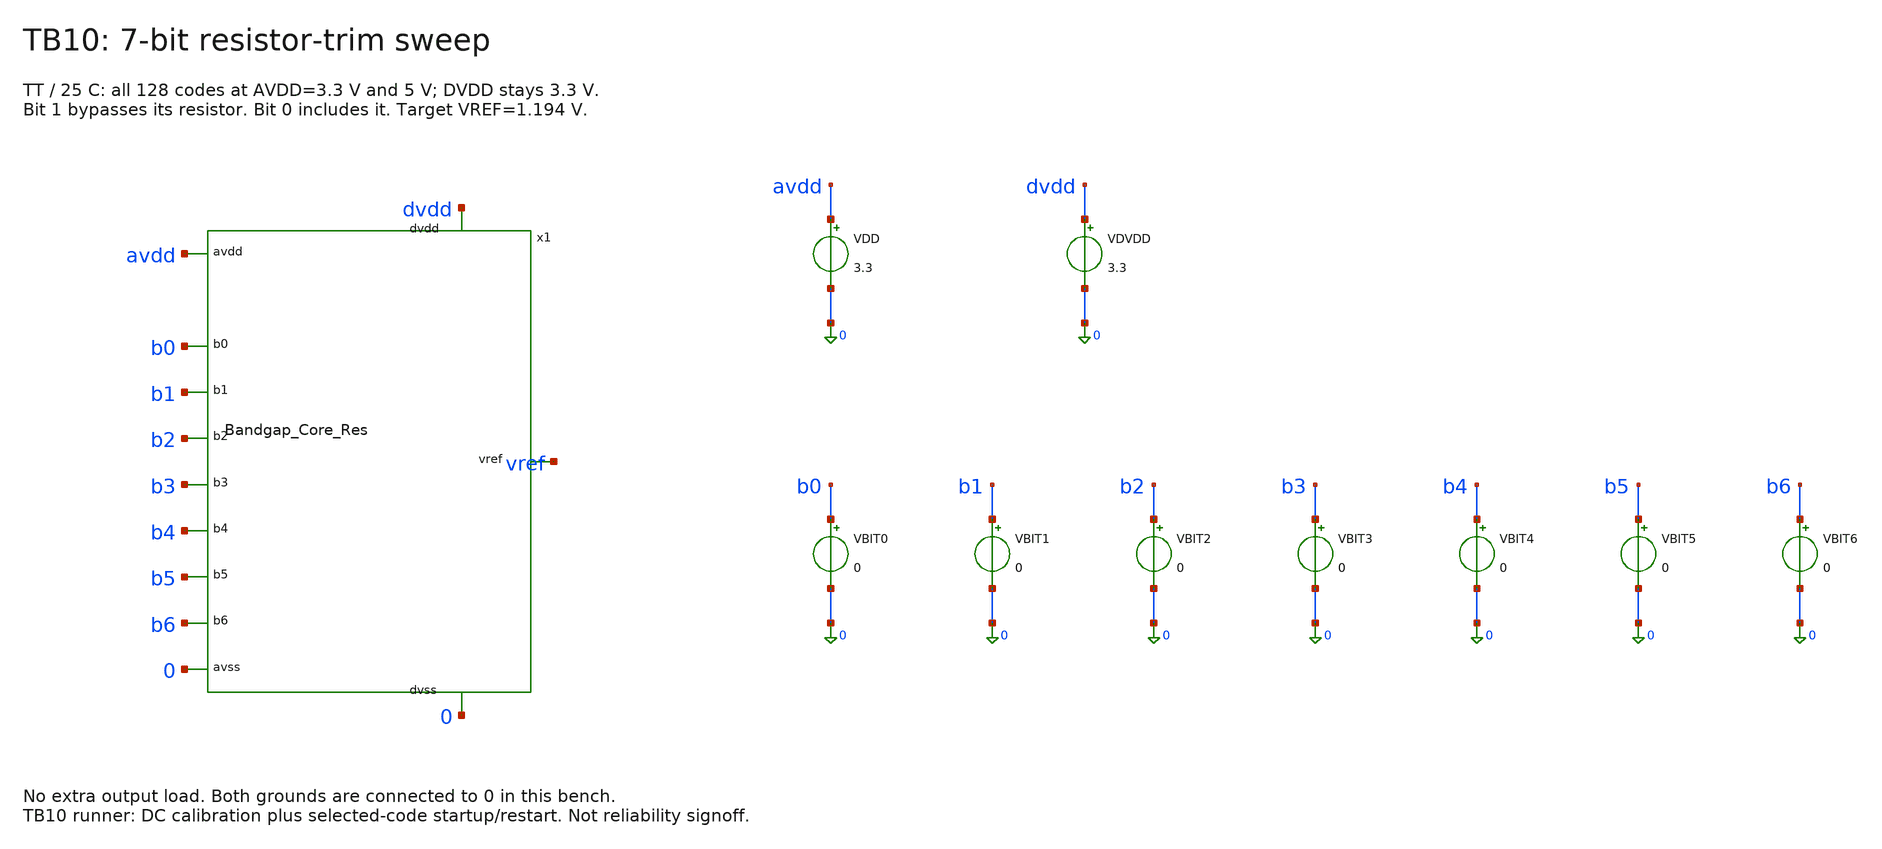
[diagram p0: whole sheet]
** sch_path: TB10_RESISTOR_TRIM.sch
**.subckt TB10_RESISTOR_TRIM
x1 avdd 0 vref b0 b1 b2 b3 b4 b5 b6 0 dvdd Bandgap_Core_Res
VDD avdd 0 3.3
VDVDD dvdd 0 3.3
VBIT0 b0 0 0
VBIT1 b1 0 0
VBIT2 b2 0 0
VBIT3 b3 0 0
VBIT4 b4 0 0
VBIT5 b5 0 0
VBIT6 b6 0 0
**** begin user architecture code

* TB_PVT_MODELS_BEGIN
.include /foss/pdks/gf180mcuD/libs.tech/ngspice/design.ngspice
.lib /foss/pdks/gf180mcuD/libs.tech/ngspice/sm141064.ngspice typical
.lib /foss/pdks/gf180mcuD/libs.tech/ngspice/sm141064.ngspice bjt_typical
.lib /foss/pdks/gf180mcuD/libs.tech/ngspice/sm141064.ngspice res_typical
* GF180 2p0fF MIM fit, charge-form ngspice compatibility implementation.
* Derived from GlobalFoundries PDK Authors (2022), Apache-2.0:
* https://github.com/google/globalfoundries-pdk-libs-gf180mcu_fd_pr
* Same geometry, voltage/temperature coefficients, leakage and corner factors.
* Differential C(V)=C0*(1+a*V+b*V^2) is implemented as
* Q(V)=C0*(V+a*V^2/2+b*V^3/3), so dQ/dV exactly equals C(V).
* This avoids ngspice's poorly scaled unity-capacitor C-expression expansion.
* Do not also include mimcap_typical: it would redefine cap_mim_2f0fF.
.param mim_corner_2p0fF=1 mc_c_cox_2p0fF=0
.subckt cap_mim_2f0fF  1 2  c_length=l  c_width=w dtemp=0 par=1
.param gleak='9.51e-10/5*10000'
.param c_cox='1.99e-3*mim_corner_2p0fF'
.param c_capsw='2.383e-10*mim_corner_2p0fF'
.param c_vcr1='0+(c_width>5u||c_length>5u)*8.742e-6+(c_width<=5u||c_length<=5u)*(-81e-6)'
.param c_vcr2='0+(c_width>5u||c_length>5u)*9.188e-6+(c_width<=5u||c_length<=5u)*(16.7e-6)'

.param c_tnom=25
.param c_tc1=1.46e-5
.param c_tc2=-5.55e-8
.param c_AREA='c_length*c_width'
.param c_PERI='2*(c_length+c_width)'

.param c_c0='(c_cox*c_AREA+c_capsw*c_PERI)*(1+c_tc1*(temper +dtemp -c_tnom)+c_tc2*(temper+dtemp-c_tnom)*(temper+dtemp-c_tnom))'
*
c_cap 1 2 Q='c_c0*(v(1,2)+c_vcr1*v(1,2)*v(1,2)/2+c_vcr2*v(1,2)*v(1,2)*v(1,2)/3)*(1+mc_c_cox_2p0fF)'
r_leak 1 2 r='1/(gleak*c_AREA)' tc1=c_tc1 tc2=c_tc2 dtemp=dtemp
.ends cap_mim_2f0fF
* Bootstrap nominal process; runner selects each corner independently. Mismatch disabled. MIM compatibility model above is intentional.
.options tnom=25 numdgt=15 method=gear maxord=2 reltol=1e-5 vntol=1e-7 abstol=1e-13 itl4=200
.param sw_stat_global=0 sw_stat_mismatch=0 fnoicor=0
.param VDD_RUN=5
.temp 25
* TB_PVT_MODELS_END


.control
set noaskquit
echo Run run_bandgap.py --configure before simulating from Xschem.
shell python3 run_bandgap.py --deck TB10_RESISTOR_TRIM.spice --test TB10_RESISTOR_TRIM
echo RUNNER_RETURNED_CHECK_REPORT_AND_ERRORS
quit
.endc

**** end user architecture code
**.ends
.end
